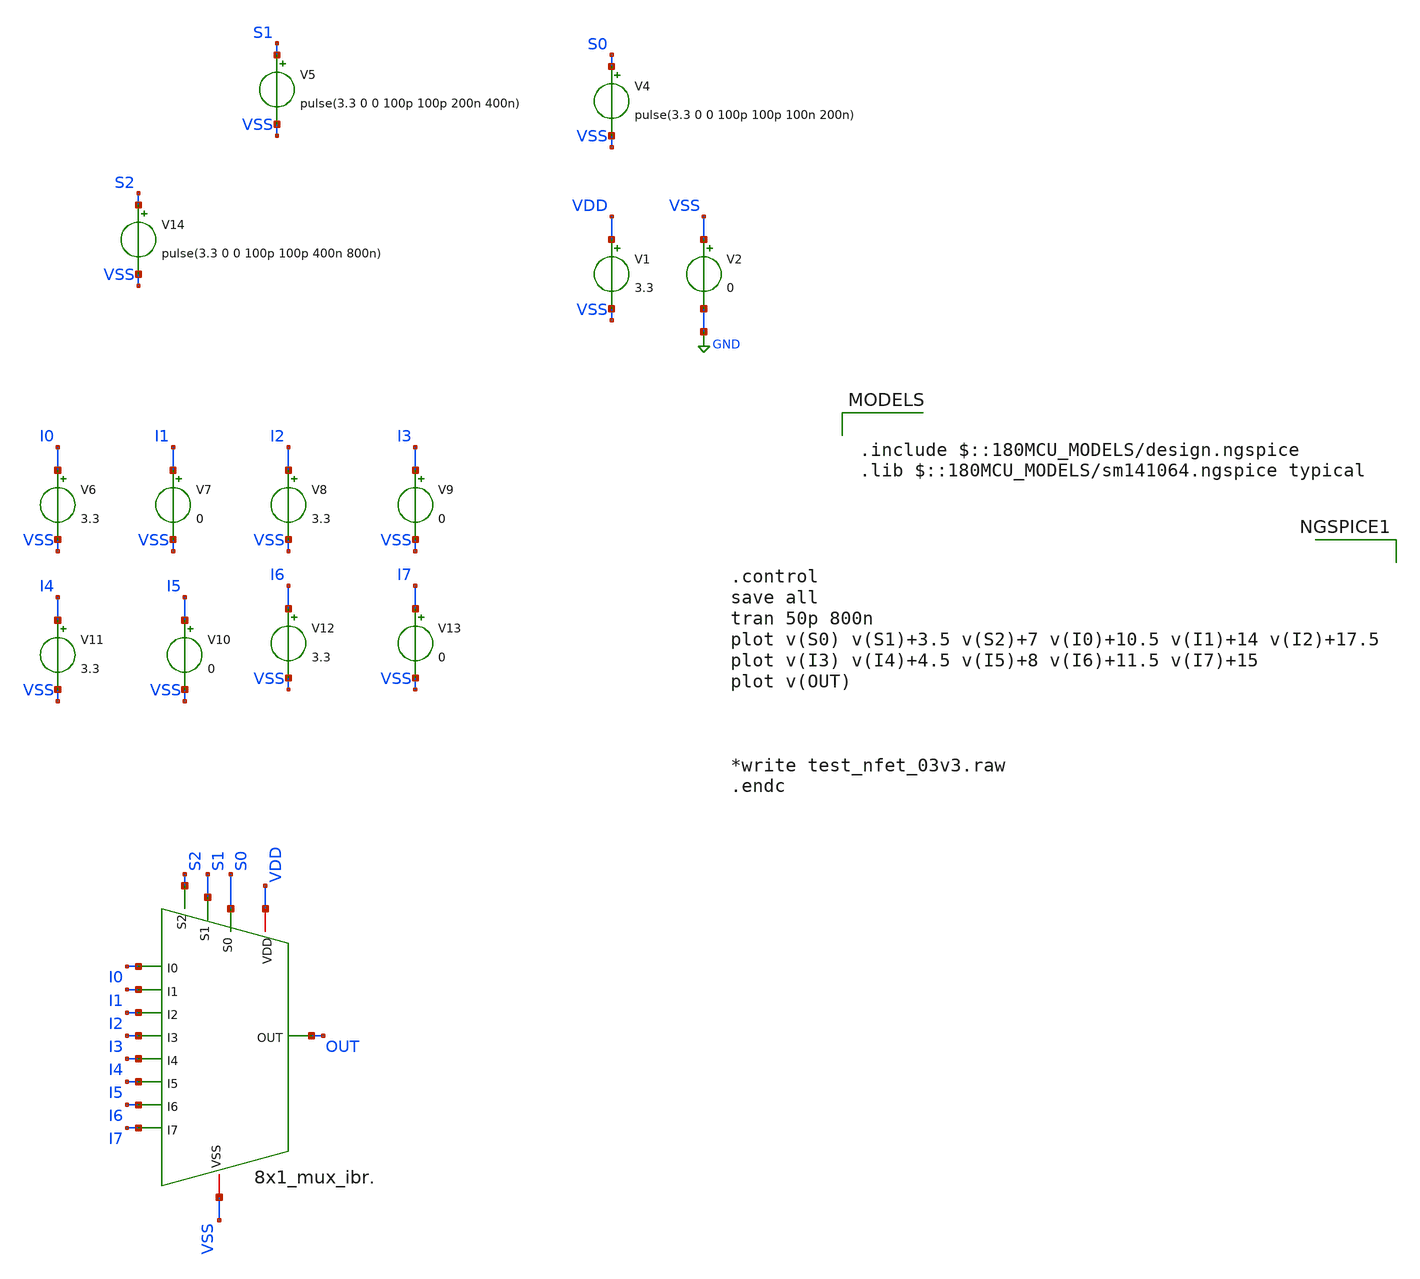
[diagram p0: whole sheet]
** sch_path: Clock_Generator_PAKISTAN_02/xschem/8x1_mux_test_ibr..sch
**.subckt 8x1_mux_test_ibr.
V1 VDD VSS 3.3
V2 VSS GND 0
V4 S0 VSS pulse(3.3 0 0 100p 100p 100n 200n)
V5 S1 VSS pulse(3.3 0 0 100p 100p 200n 400n)
V6 I0 VSS 3.3
V7 I1 VSS 0
V8 I2 VSS 3.3
V9 I3 VSS 0
V10 I5 VSS 0
V11 I4 VSS 3.3
V12 I6 VSS 3.3
V13 I7 VSS 0
V14 S2 VSS pulse(3.3 0 0 100p 100p 400n 800n)
x2 VDD VSS S1 S0 OUT S2 I0 I7 I3 I2 I5 I1 I4 I6 8x1_mux_ibr.
**** begin user architecture code

.include $::180MCU_MODELS/design.ngspice
.lib $::180MCU_MODELS/sm141064.ngspice typical



.control
save all
tran 50p 800n
plot v(S0) v(S1)+3.5 v(S2)+7 v(I0)+10.5 v(I1)+14 v(I2)+17.5
plot v(I3) v(I4)+4.5 v(I5)+8 v(I6)+11.5 v(I7)+15
plot v(OUT)



*write test_nfet_03v3.raw
.endc


**** end user architecture code
**.ends
.GLOBAL GND
.end
